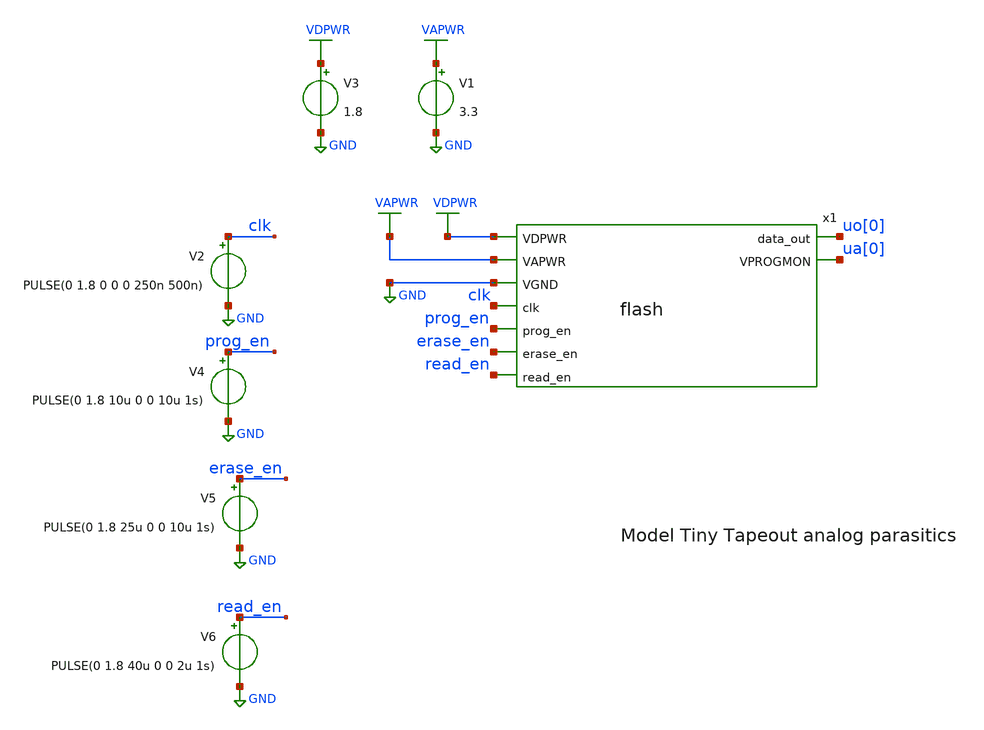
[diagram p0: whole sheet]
** sch_path: xschem/flash_tb.sch
**.subckt flash_tb
V1 VAPWR GND 3.3
V2 clk GND PULSE(0 1.8 0 0 0 250n 500n)
x1 uo[0] VDPWR VAPWR GND clk ua[0] prog_en erase_en read_en flash
V3 VDPWR GND 1.8
V4 prog_en GND PULSE(0 1.8 10u 0 0 10u 1s)
V5 erase_en GND PULSE(0 1.8 25u 0 0 10u 1s)
V6 read_en GND PULSE(0 1.8 40u 0 0 2u 1s)
**** begin user architecture code

** opencircuitdesign pdks install
.lib $::SKYWATER_MODELS/sky130.lib.spice tt
.include $::SKYWATER_MODELS/sonos_see_e/begin_of_life.pm3.spice
.include $::SKYWATER_MODELS/sonos_see_e/begin_of_life.spice





.tran 10n 100u
.save all

.control
run
write flash_tb.raw
.endc


**** end user architecture code
**.ends
.GLOBAL GND
.GLOBAL VAPWR
.GLOBAL VDPWR
.end
